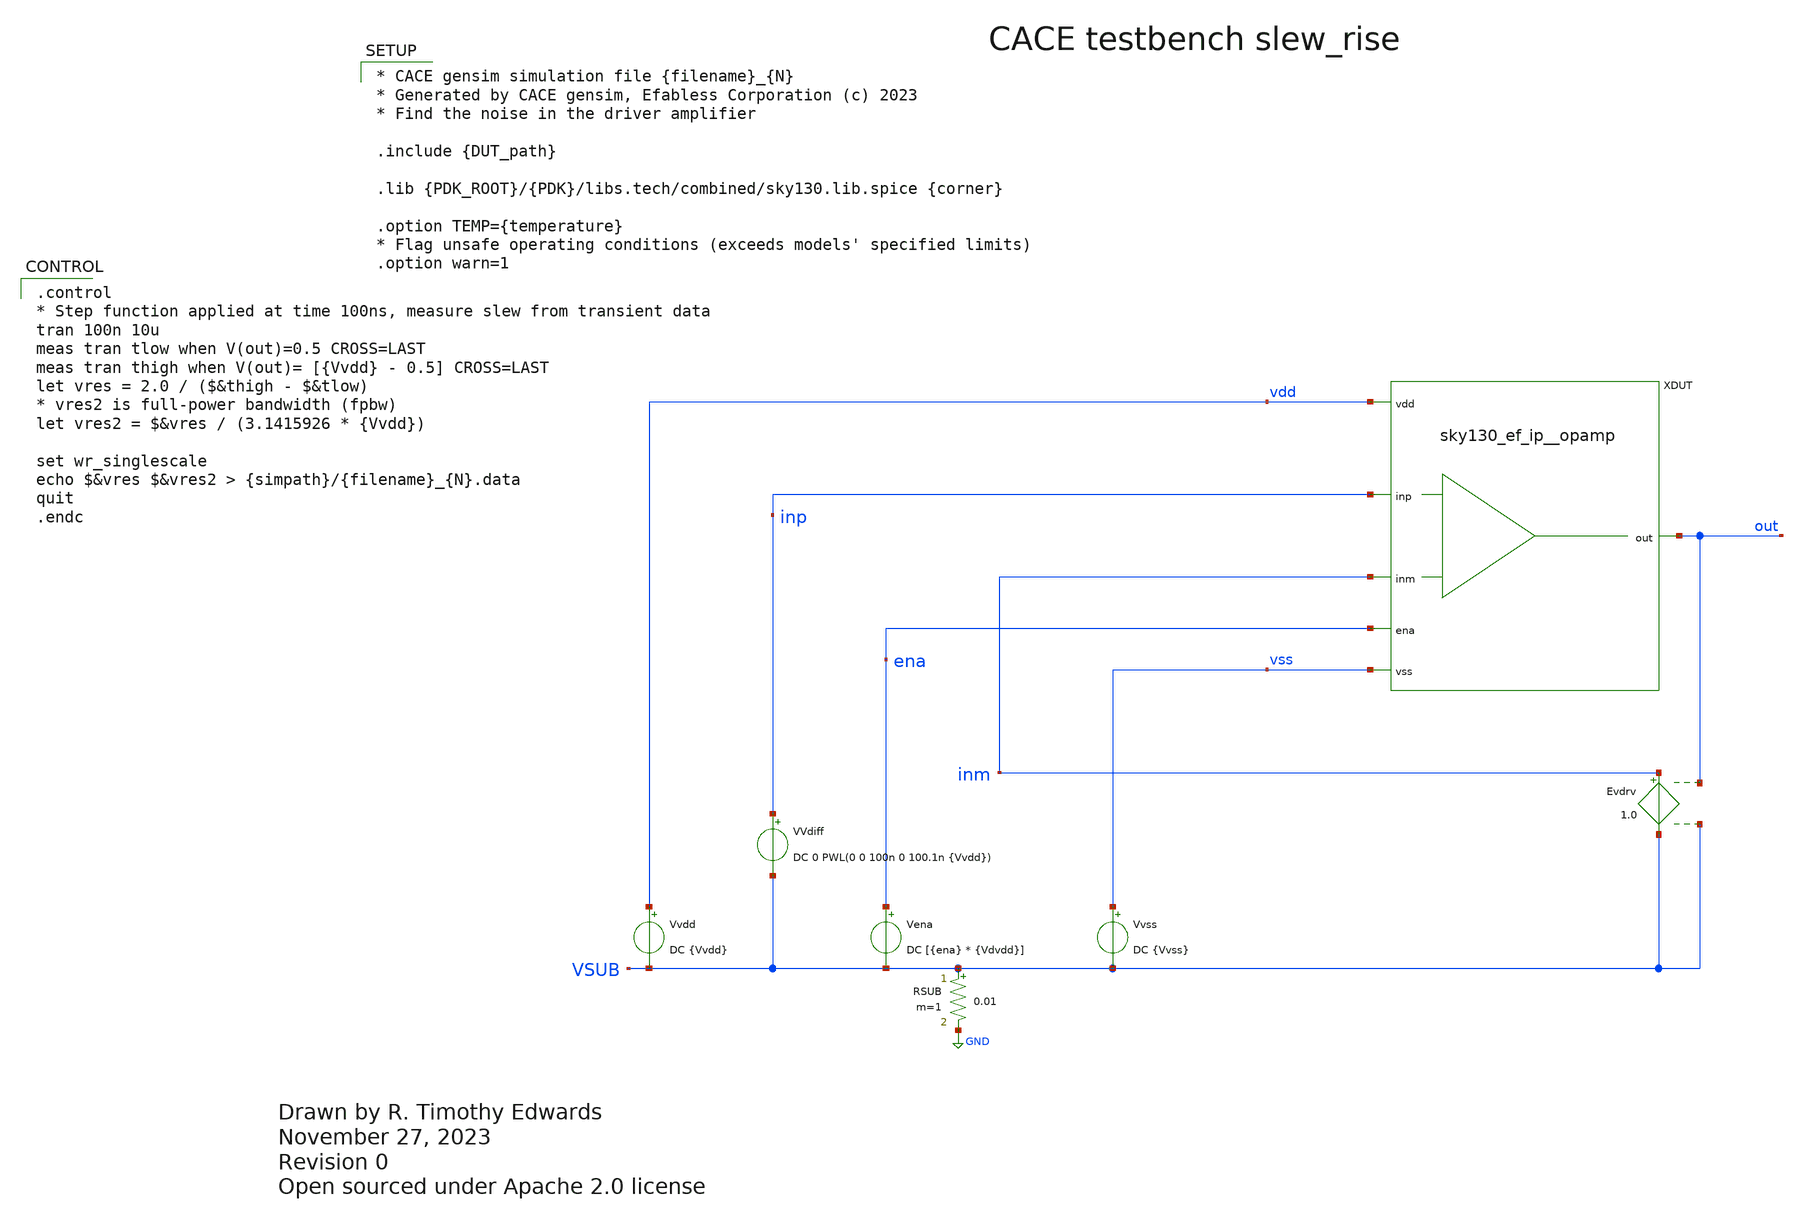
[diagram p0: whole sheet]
** sch_path: cace/templates/slew_rise.sch
* Open sourced under Apache 2.0 license
**.subckt slew_rise
VVdiff inp VSUB DC 0 PWL(0 0 100n 0 100.1n {Vvdd})
Vena ena VSUB DC [{ena} * {Vdvdd}]
Vvss vss VSUB DC {Vvss}
Vvdd vdd VSUB DC {Vvdd}
RSUB VSUB GND 0.01 m=1
XDUT vdd out ena vss inp inm sky130_ef_ip__opamp
Evdrv inm VSUB out VSUB 1.0
**** begin user architecture code

.control
* Step function applied at time 100ns, measure slew from transient data
tran 100n 10u
meas tran tlow when V(out)=0.5 CROSS=LAST
meas tran thigh when V(out)= [{Vvdd} - 0.5] CROSS=LAST
let vres = 2.0 / ($&thigh - $&tlow)
* vres2 is full-power bandwidth (fpbw)
let vres2 = $&vres / (3.1415926 * {Vvdd})

set wr_singlescale
echo $&vres $&vres2 > {simpath}/{filename}_{N}.data
quit
.endc



* CACE gensim simulation file {filename}_{N}
* Generated by CACE gensim, Efabless Corporation (c) 2023
* Find the noise in the driver amplifier

.include {DUT_path}

.lib {PDK_ROOT}/{PDK}/libs.tech/combined/sky130.lib.spice {corner}

.option TEMP={temperature}
* Flag unsafe operating conditions (exceeds models' specified limits)
.option warn=1


**** end user architecture code
**.ends

* expanding   symbol:  sky130_ef_ip__opamp.sym # of pins=6
** sym_path: xschem/sky130_ef_ip__opamp.sym
** sch_path: xschem/sky130_ef_ip__opamp.sch
.subckt sky130_ef_ip__opamp vdd out ena vss inp inm
*.ipin inp
*.ipin vdd
*.ipin vss
*.opin out
*.ipin ena
*.ipin inm
XM4 pdrv1 net1 vdd vdd sky130_fd_pr__pfet_g5v0d10v5 L=0.5 W=2 nf=2 ad='int((nf+1)/2) * W/nf * 0.29' as='int((nf+2)/2)
+ * W/nf * 0.29' pd='2*int((nf+1)/2) * (W/nf + 0.29)' ps='2*int((nf+2)/2) * (W/nf + 0.29)' nrd='0.29 /
+ W' nrs='0.29 / W' sa=0 sb=0 sd=0 mult=1 m=1
XM5 vdd net1 net1 vdd sky130_fd_pr__pfet_g5v0d10v5 L=0.5 W=2 nf=2 ad='int((nf+1)/2) * W/nf * 0.29' as='int((nf+2)/2)
+ * W/nf * 0.29' pd='2*int((nf+1)/2) * (W/nf + 0.29)' ps='2*int((nf+2)/2) * (W/nf + 0.29)' nrd='0.29 /
+ W' nrs='0.29 / W' sa=0 sb=0 sd=0 mult=1 m=1
XM9 vcomn1 nbias vss vss sky130_fd_pr__nfet_g5v0d10v5 L=0.5 W=1 nf=1 ad='int((nf+1)/2) * W/nf * 0.29' as='int((nf+2)/2)
+ * W/nf * 0.29' pd='2*int((nf+1)/2) * (W/nf + 0.29)' ps='2*int((nf+2)/2) * (W/nf + 0.29)' nrd='0.29 /
+ W' nrs='0.29 / W' sa=0 sb=0 sd=0 mult=1 m=1
XM10 vss nbias nbias vss sky130_fd_pr__nfet_g5v0d10v5 L=0.5 W=4 nf=4 ad='int((nf+1)/2) * W/nf * 0.29' as='int((nf+2)/2)
+ * W/nf * 0.29' pd='2*int((nf+1)/2) * (W/nf + 0.29)' ps='2*int((nf+2)/2) * (W/nf + 0.29)' nrd='0.29 /
+ W' nrs='0.29 / W' sa=0 sb=0 sd=0 mult=1 m=1
XR1 net4 vdd vss sky130_fd_pr__res_xhigh_po_0p35 L=100 mult=1 m=1
XM20 out pdrv1 vdd vdd sky130_fd_pr__pfet_g5v0d10v5 L=0.5 W=200 nf=200 ad='int((nf+1)/2) * W/nf * 0.29' as='int((nf+2)/2)
+ * W/nf * 0.29' pd='2*int((nf+1)/2) * (W/nf + 0.29)' ps='2*int((nf+2)/2) * (W/nf + 0.29)' nrd='0.29 /
+ W' nrs='0.29 / W' sa=0 sb=0 sd=0 mult=1 m=1
XM22 out ndrv vss vss sky130_fd_pr__nfet_g5v0d10v5 L=0.5 W=120 nf=120 ad='int((nf+1)/2) * W/nf * 0.29' as='int((nf+2)/2)
+ * W/nf * 0.29' pd='2*int((nf+1)/2) * (W/nf + 0.29)' ps='2*int((nf+2)/2) * (W/nf + 0.29)' nrd='0.29 /
+ W' nrs='0.29 / W' sa=0 sb=0 sd=0 mult=1 m=1
XM24 pbias nbias vss vss sky130_fd_pr__nfet_g5v0d10v5 L=0.5 W=1 nf=1 ad='int((nf+1)/2) * W/nf * 0.29' as='int((nf+2)/2)
+ * W/nf * 0.29' pd='2*int((nf+1)/2) * (W/nf + 0.29)' ps='2*int((nf+2)/2) * (W/nf + 0.29)' nrd='0.29 /
+ W' nrs='0.29 / W' sa=0 sb=0 sd=0 mult=1 m=1
XM25 vdd pbias pbias vdd sky130_fd_pr__pfet_g5v0d10v5 L=0.5 W=1 nf=1 ad='int((nf+1)/2) * W/nf * 0.29' as='int((nf+2)/2)
+ * W/nf * 0.29' pd='2*int((nf+1)/2) * (W/nf + 0.29)' ps='2*int((nf+2)/2) * (W/nf + 0.29)' nrd='0.29 /
+ W' nrs='0.29 / W' sa=0 sb=0 sd=0 mult=1 m=1
XM26 vcomp pbias vdd vdd sky130_fd_pr__pfet_g5v0d10v5 L=0.5 W=2 nf=2 ad='int((nf+1)/2) * W/nf * 0.29' as='int((nf+2)/2)
+ * W/nf * 0.29' pd='2*int((nf+1)/2) * (W/nf + 0.29)' ps='2*int((nf+2)/2) * (W/nf + 0.29)' nrd='0.29 /
+ W' nrs='0.29 / W' sa=0 sb=0 sd=0 mult=1 m=1
XM27 net2 inm vcomp vdd sky130_fd_pr__pfet_g5v0d10v5 L=0.5 W=2 nf=2 ad='int((nf+1)/2) * W/nf * 0.29' as='int((nf+2)/2)
+ * W/nf * 0.29' pd='2*int((nf+1)/2) * (W/nf + 0.29)' ps='2*int((nf+2)/2) * (W/nf + 0.29)' nrd='0.29 /
+ W' nrs='0.29 / W' sa=0 sb=0 sd=0 mult=1 m=1
XM28 vcomp inp ndrv vdd sky130_fd_pr__pfet_g5v0d10v5 L=0.5 W=2 nf=2 ad='int((nf+1)/2) * W/nf * 0.29' as='int((nf+2)/2)
+ * W/nf * 0.29' pd='2*int((nf+1)/2) * (W/nf + 0.29)' ps='2*int((nf+2)/2) * (W/nf + 0.29)' nrd='0.29 /
+ W' nrs='0.29 / W' sa=0 sb=0 sd=0 mult=1 m=1
XM29 ndrv net2 vss vss sky130_fd_pr__nfet_g5v0d10v5 L=0.5 W=1 nf=1 ad='int((nf+1)/2) * W/nf * 0.29' as='int((nf+2)/2)
+ * W/nf * 0.29' pd='2*int((nf+1)/2) * (W/nf + 0.29)' ps='2*int((nf+2)/2) * (W/nf + 0.29)' nrd='0.29 /
+ W' nrs='0.29 / W' sa=0 sb=0 sd=0 mult=1 m=1
XM30 vss net2 net2 vss sky130_fd_pr__nfet_g5v0d10v5 L=0.5 W=1 nf=1 ad='int((nf+1)/2) * W/nf * 0.29' as='int((nf+2)/2)
+ * W/nf * 0.29' pd='2*int((nf+1)/2) * (W/nf + 0.29)' ps='2*int((nf+2)/2) * (W/nf + 0.29)' nrd='0.29 /
+ W' nrs='0.29 / W' sa=0 sb=0 sd=0 mult=1 m=1
XM1 net1 inm vcomn1 vss sky130_fd_pr__nfet_g5v0d10v5 L=0.5 W=1 nf=1 ad='int((nf+1)/2) * W/nf * 0.29' as='int((nf+2)/2)
+ * W/nf * 0.29' pd='2*int((nf+1)/2) * (W/nf + 0.29)' ps='2*int((nf+2)/2) * (W/nf + 0.29)' nrd='0.29 /
+ W' nrs='0.29 / W' sa=0 sb=0 sd=0 mult=1 m=1
XM2 vcomn1 inp pdrv1 vss sky130_fd_pr__nfet_g5v0d10v5 L=0.5 W=1 nf=1 ad='int((nf+1)/2) * W/nf * 0.29' as='int((nf+2)/2)
+ * W/nf * 0.29' pd='2*int((nf+1)/2) * (W/nf + 0.29)' ps='2*int((nf+2)/2) * (W/nf + 0.29)' nrd='0.29 /
+ W' nrs='0.29 / W' sa=0 sb=0 sd=0 mult=1 m=1
XM3 pdrv2 net3 vdd vdd sky130_fd_pr__pfet_g5v0d10v5 L=0.5 W=2 nf=2 ad='int((nf+1)/2) * W/nf * 0.29' as='int((nf+2)/2)
+ * W/nf * 0.29' pd='2*int((nf+1)/2) * (W/nf + 0.29)' ps='2*int((nf+2)/2) * (W/nf + 0.29)' nrd='0.29 /
+ W' nrs='0.29 / W' sa=0 sb=0 sd=0 mult=1 m=1
XM6 vdd net3 net3 vdd sky130_fd_pr__pfet_g5v0d10v5 L=0.5 W=2 nf=2 ad='int((nf+1)/2) * W/nf * 0.29' as='int((nf+2)/2)
+ * W/nf * 0.29' pd='2*int((nf+1)/2) * (W/nf + 0.29)' ps='2*int((nf+2)/2) * (W/nf + 0.29)' nrd='0.29 /
+ W' nrs='0.29 / W' sa=0 sb=0 sd=0 mult=1 m=1
XM7 vcomn2 nbias vss vss sky130_fd_pr__nfet_g5v0d10v5 L=0.5 W=1 nf=1 ad='int((nf+1)/2) * W/nf * 0.29' as='int((nf+2)/2)
+ * W/nf * 0.29' pd='2*int((nf+1)/2) * (W/nf + 0.29)' ps='2*int((nf+2)/2) * (W/nf + 0.29)' nrd='0.29 /
+ W' nrs='0.29 / W' sa=0 sb=0 sd=0 mult=1 m=1
XM8 net3 inm vcomn2 vss sky130_fd_pr__nfet_03v3_nvt L=0.5 W=1 nf=1 ad='int((nf+1)/2) * W/nf * 0.29' as='int((nf+2)/2)
+ * W/nf * 0.29' pd='2*int((nf+1)/2) * (W/nf + 0.29)' ps='2*int((nf+2)/2) * (W/nf + 0.29)' nrd='0.29 /
+ W' nrs='0.29 / W' sa=0 sb=0 sd=0 mult=1 m=1
XM11 vcomn2 inp pdrv2 vss sky130_fd_pr__nfet_03v3_nvt L=0.5 W=1 nf=1 ad='int((nf+1)/2) * W/nf * 0.29' as='int((nf+2)/2)
+ * W/nf * 0.29' pd='2*int((nf+1)/2) * (W/nf + 0.29)' ps='2*int((nf+2)/2) * (W/nf + 0.29)' nrd='0.29 /
+ W' nrs='0.29 / W' sa=0 sb=0 sd=0 mult=1 m=1
XM12 vdd pdrv2 out vdd sky130_fd_pr__pfet_g5v0d10v5 L=0.5 W=200 nf=200 ad='int((nf+1)/2) * W/nf * 0.29' as='int((nf+2)/2)
+ * W/nf * 0.29' pd='2*int((nf+1)/2) * (W/nf + 0.29)' ps='2*int((nf+2)/2) * (W/nf + 0.29)' nrd='0.29 /
+ W' nrs='0.29 / W' sa=0 sb=0 sd=0 mult=1 m=1
XXD1 vss inp sky130_fd_pr__diode_pw2nd_05v5 area=3.6e11 pj=4e6
XM13 net4 ena nbias vss sky130_fd_pr__nfet_g5v0d10v5 L=0.5 W=1 nf=1 ad='int((nf+1)/2) * W/nf * 0.29' as='int((nf+2)/2)
+ * W/nf * 0.29' pd='2*int((nf+1)/2) * (W/nf + 0.29)' ps='2*int((nf+2)/2) * (W/nf + 0.29)' nrd='0.29 /
+ W' nrs='0.29 / W' sa=0 sb=0 sd=0 mult=1 m=1
XXD2 vss ena sky130_fd_pr__diode_pw2nd_05v5 area=3.6e11 pj=4e6
XXD3 vss inm sky130_fd_pr__diode_pw2nd_05v5 area=3.6e11 pj=4e6
.ends

.GLOBAL GND
.end
